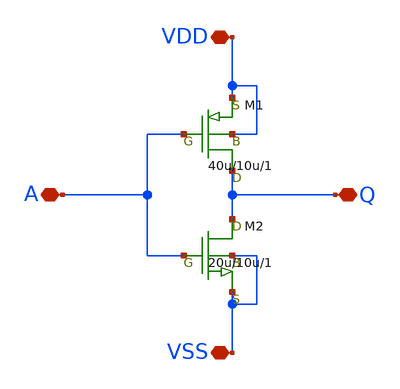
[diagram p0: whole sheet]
** sch_path: Submitted/inverter_pine-4.sch
**.subckt inverter_pine-4 VDD A Q VSS
*.iopin VDD
*.iopin A
*.iopin Q
*.iopin VSS
M1 Q A VDD VDD pch w=40u l=10u as=0 ps=0 ad=0 pd=0 m=1
M2 Q A VSS VSS nch w=20u l=10u as=0 ps=0 ad=0 pd=0 m=1
**.ends
.end
